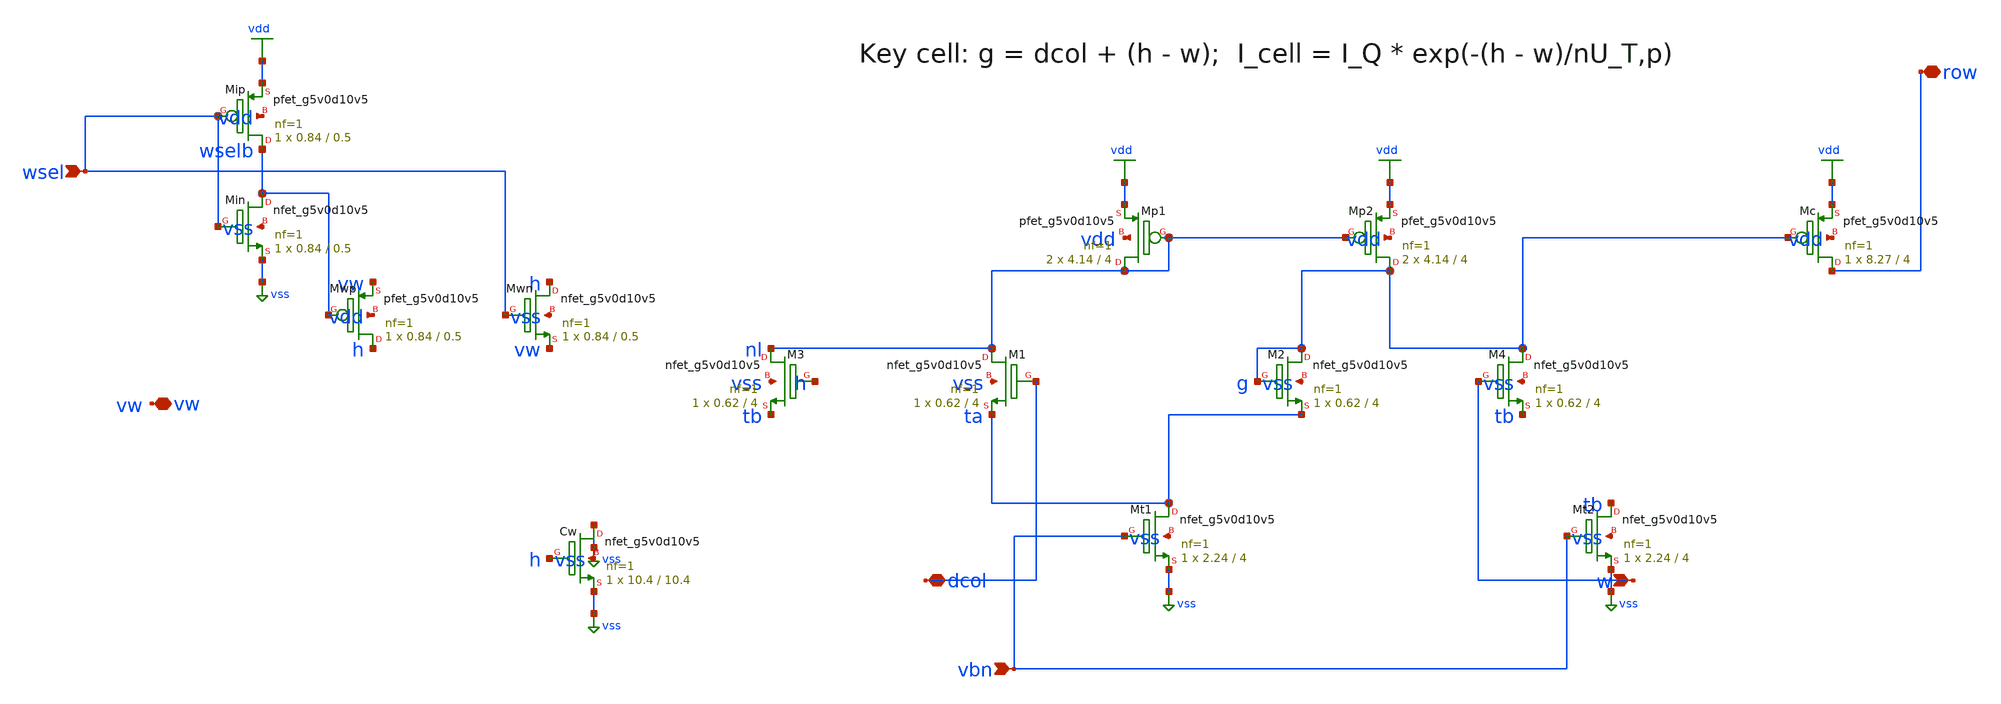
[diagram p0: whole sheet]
** sch_path: xschem/rt5w_keycell.sch
**.subckt rt5w_keycell dcol w vw wsel vbn row
*.iopin dcol
*.ipin w
*.iopin vw
*.ipin wsel
*.ipin vbn
*.iopin row
XMp1 nl nl vdd vdd sky130_fd_pr__pfet_g5v0d10v5 L=4 W=4.14 nf=1 ad=1.201 as=1.201 pd=8.86 ps=8.86
+ nrd=0.07005 nrs=0.07005 sa=0 sb=0 sd=0 mult=2 m=2
XMp2 g nl vdd vdd sky130_fd_pr__pfet_g5v0d10v5 L=4 W=4.14 nf=1 ad=1.201 as=1.201 pd=8.86 ps=8.86
+ nrd=0.07005 nrs=0.07005 sa=0 sb=0 sd=0 mult=2 m=2
XM1 nl dcol ta vss sky130_fd_pr__nfet_g5v0d10v5 L=4 W=0.62 nf=1 ad=0.1798 as=0.1798 pd=1.82 ps=1.82
+ nrd=0.4677 nrs=0.4677 sa=0 sb=0 sd=0 mult=1 m=1
XM2 g g ta vss sky130_fd_pr__nfet_g5v0d10v5 L=4 W=0.62 nf=1 ad=0.1798 as=0.1798 pd=1.82 ps=1.82
+ nrd=0.4677 nrs=0.4677 sa=0 sb=0 sd=0 mult=1 m=1
XM3 nl h tb vss sky130_fd_pr__nfet_g5v0d10v5 L=4 W=0.62 nf=1 ad=0.1798 as=0.1798 pd=1.82 ps=1.82
+ nrd=0.4677 nrs=0.4677 sa=0 sb=0 sd=0 mult=1 m=1
XM4 g w tb vss sky130_fd_pr__nfet_g5v0d10v5 L=4 W=0.62 nf=1 ad=0.1798 as=0.1798 pd=1.82 ps=1.82
+ nrd=0.4677 nrs=0.4677 sa=0 sb=0 sd=0 mult=1 m=1
XMt1 ta vbn vss vss sky130_fd_pr__nfet_g5v0d10v5 L=4 W=2.24 nf=1 ad=0.6496 as=0.6496 pd=5.06 ps=5.06
+ nrd=0.1295 nrs=0.1295 sa=0 sb=0 sd=0 mult=1 m=1
XMt2 tb vbn vss vss sky130_fd_pr__nfet_g5v0d10v5 L=4 W=2.24 nf=1 ad=0.6496 as=0.6496 pd=5.06 ps=5.06
+ nrd=0.1295 nrs=0.1295 sa=0 sb=0 sd=0 mult=1 m=1
XMc row g vdd vdd sky130_fd_pr__pfet_g5v0d10v5 L=4 W=8.27 nf=1 ad=2.398 as=2.398 pd=17.12 ps=17.12
+ nrd=0.03507 nrs=0.03507 sa=0 sb=0 sd=0 mult=1 m=1
XCw vss h vss vss sky130_fd_pr__nfet_g5v0d10v5 L=10.4 W=10.4 nf=1 ad=3.016 as=3.016 pd=21.38
+ ps=21.38 nrd=0.02788 nrs=0.02788 sa=0 sb=0 sd=0 mult=1 m=1
XMwn h wsel vw vss sky130_fd_pr__nfet_g5v0d10v5 L=0.5 W=0.84 nf=1 ad=0.2436 as=0.2436 pd=2.26
+ ps=2.26 nrd=0.3452 nrs=0.3452 sa=0 sb=0 sd=0 mult=1 m=1
XMwp h wselb vw vdd sky130_fd_pr__pfet_g5v0d10v5 L=0.5 W=0.84 nf=1 ad=0.2436 as=0.2436 pd=2.26
+ ps=2.26 nrd=0.3452 nrs=0.3452 sa=0 sb=0 sd=0 mult=1 m=1
XMip wselb wsel vdd vdd sky130_fd_pr__pfet_g5v0d10v5 L=0.5 W=0.84 nf=1 ad=0.2436 as=0.2436 pd=2.26
+ ps=2.26 nrd=0.3452 nrs=0.3452 sa=0 sb=0 sd=0 mult=1 m=1
XMin wselb wsel vss vss sky130_fd_pr__nfet_g5v0d10v5 L=0.5 W=0.84 nf=1 ad=0.2436 as=0.2436 pd=2.26
+ ps=2.26 nrd=0.3452 nrs=0.3452 sa=0 sb=0 sd=0 mult=1 m=1
**.ends
.GLOBAL vdd
.GLOBAL vss
.end
